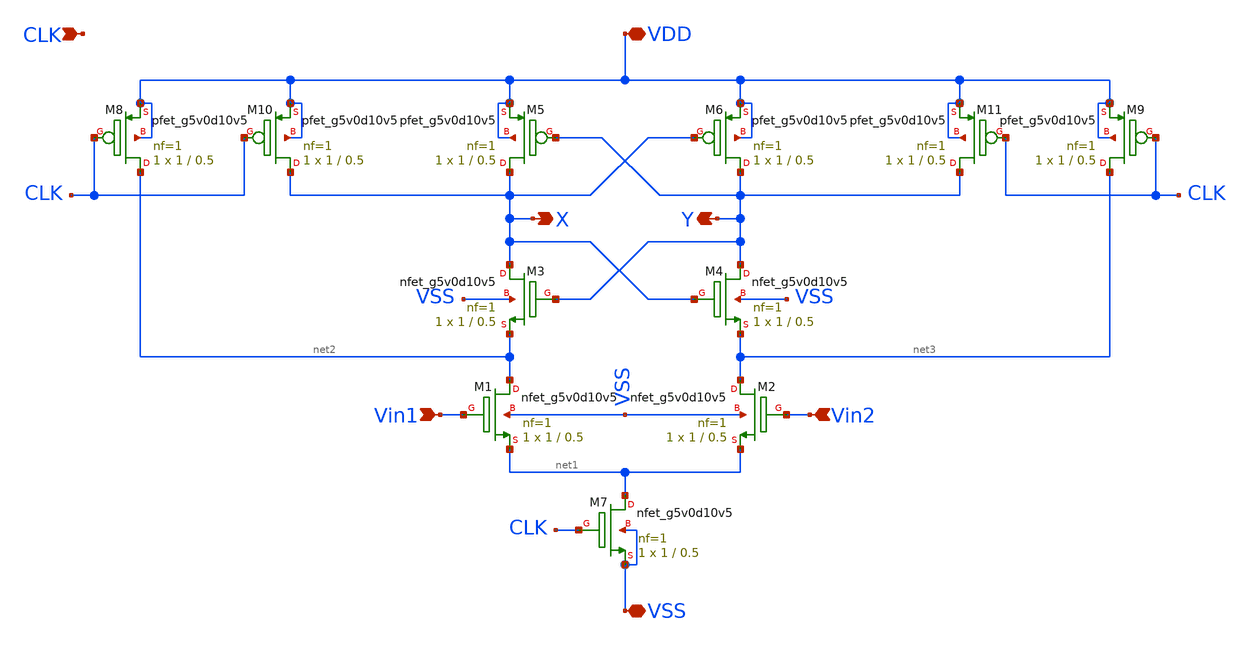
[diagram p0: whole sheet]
** sch_path: xschem/comparator/comparator.sch
**.subckt comparator VDD VSS Vin1 Vin2 X Y CLK
*.iopin VDD
*.iopin VSS
*.ipin Vin1
*.ipin Vin2
*.opin X
*.opin Y
*.ipin CLK
XM1 net2 Vin1 net1 VSS sky130_fd_pr__nfet_g5v0d10v5 L=0.5 W=1 nf=1 ad='int((nf+1)/2) * W/nf * 0.29' as='int((nf+2)/2) * W/nf * 0.29'
+ pd='2*int((nf+1)/2) * (W/nf + 0.29)' ps='2*int((nf+2)/2) * (W/nf + 0.29)' nrd='0.29 / W' nrs='0.29 / W'
+ sa=0 sb=0 sd=0 mult=1 m=1
XM2 net3 Vin2 net1 VSS sky130_fd_pr__nfet_g5v0d10v5 L=0.5 W=1 nf=1 ad='int((nf+1)/2) * W/nf * 0.29' as='int((nf+2)/2) * W/nf * 0.29'
+ pd='2*int((nf+1)/2) * (W/nf + 0.29)' ps='2*int((nf+2)/2) * (W/nf + 0.29)' nrd='0.29 / W' nrs='0.29 / W'
+ sa=0 sb=0 sd=0 mult=1 m=1
XM3 X Y net2 VSS sky130_fd_pr__nfet_g5v0d10v5 L=0.5 W=1 nf=1 ad='int((nf+1)/2) * W/nf * 0.29' as='int((nf+2)/2) * W/nf * 0.29'
+ pd='2*int((nf+1)/2) * (W/nf + 0.29)' ps='2*int((nf+2)/2) * (W/nf + 0.29)' nrd='0.29 / W' nrs='0.29 / W'
+ sa=0 sb=0 sd=0 mult=1 m=1
XM4 Y X net3 VSS sky130_fd_pr__nfet_g5v0d10v5 L=0.5 W=1 nf=1 ad='int((nf+1)/2) * W/nf * 0.29' as='int((nf+2)/2) * W/nf * 0.29'
+ pd='2*int((nf+1)/2) * (W/nf + 0.29)' ps='2*int((nf+2)/2) * (W/nf + 0.29)' nrd='0.29 / W' nrs='0.29 / W'
+ sa=0 sb=0 sd=0 mult=1 m=1
XM5 X Y VDD VDD sky130_fd_pr__pfet_g5v0d10v5 L=0.5 W=1 nf=1 ad='int((nf+1)/2) * W/nf * 0.29' as='int((nf+2)/2) * W/nf * 0.29'
+ pd='2*int((nf+1)/2) * (W/nf + 0.29)' ps='2*int((nf+2)/2) * (W/nf + 0.29)' nrd='0.29 / W' nrs='0.29 / W'
+ sa=0 sb=0 sd=0 mult=1 m=1
XM6 Y X VDD VDD sky130_fd_pr__pfet_g5v0d10v5 L=0.5 W=1 nf=1 ad='int((nf+1)/2) * W/nf * 0.29' as='int((nf+2)/2) * W/nf * 0.29'
+ pd='2*int((nf+1)/2) * (W/nf + 0.29)' ps='2*int((nf+2)/2) * (W/nf + 0.29)' nrd='0.29 / W' nrs='0.29 / W'
+ sa=0 sb=0 sd=0 mult=1 m=1
XM7 net1 CLK VSS VSS sky130_fd_pr__nfet_g5v0d10v5 L=0.5 W=1 nf=1 ad='int((nf+1)/2) * W/nf * 0.29' as='int((nf+2)/2) * W/nf * 0.29'
+ pd='2*int((nf+1)/2) * (W/nf + 0.29)' ps='2*int((nf+2)/2) * (W/nf + 0.29)' nrd='0.29 / W' nrs='0.29 / W'
+ sa=0 sb=0 sd=0 mult=1 m=1
XM8 net2 CLK VDD VDD sky130_fd_pr__pfet_g5v0d10v5 L=0.5 W=1 nf=1 ad='int((nf+1)/2) * W/nf * 0.29' as='int((nf+2)/2) * W/nf * 0.29'
+ pd='2*int((nf+1)/2) * (W/nf + 0.29)' ps='2*int((nf+2)/2) * (W/nf + 0.29)' nrd='0.29 / W' nrs='0.29 / W'
+ sa=0 sb=0 sd=0 mult=1 m=1
XM9 net3 CLK VDD VDD sky130_fd_pr__pfet_g5v0d10v5 L=0.5 W=1 nf=1 ad='int((nf+1)/2) * W/nf * 0.29' as='int((nf+2)/2) * W/nf * 0.29'
+ pd='2*int((nf+1)/2) * (W/nf + 0.29)' ps='2*int((nf+2)/2) * (W/nf + 0.29)' nrd='0.29 / W' nrs='0.29 / W'
+ sa=0 sb=0 sd=0 mult=1 m=1
XM10 X CLK VDD VDD sky130_fd_pr__pfet_g5v0d10v5 L=0.5 W=1 nf=1 ad='int((nf+1)/2) * W/nf * 0.29' as='int((nf+2)/2) * W/nf * 0.29'
+ pd='2*int((nf+1)/2) * (W/nf + 0.29)' ps='2*int((nf+2)/2) * (W/nf + 0.29)' nrd='0.29 / W' nrs='0.29 / W'
+ sa=0 sb=0 sd=0 mult=1 m=1
XM11 Y CLK VDD VDD sky130_fd_pr__pfet_g5v0d10v5 L=0.5 W=1 nf=1 ad='int((nf+1)/2) * W/nf * 0.29' as='int((nf+2)/2) * W/nf * 0.29'
+ pd='2*int((nf+1)/2) * (W/nf + 0.29)' ps='2*int((nf+2)/2) * (W/nf + 0.29)' nrd='0.29 / W' nrs='0.29 / W'
+ sa=0 sb=0 sd=0 mult=1 m=1
**.ends
.end
